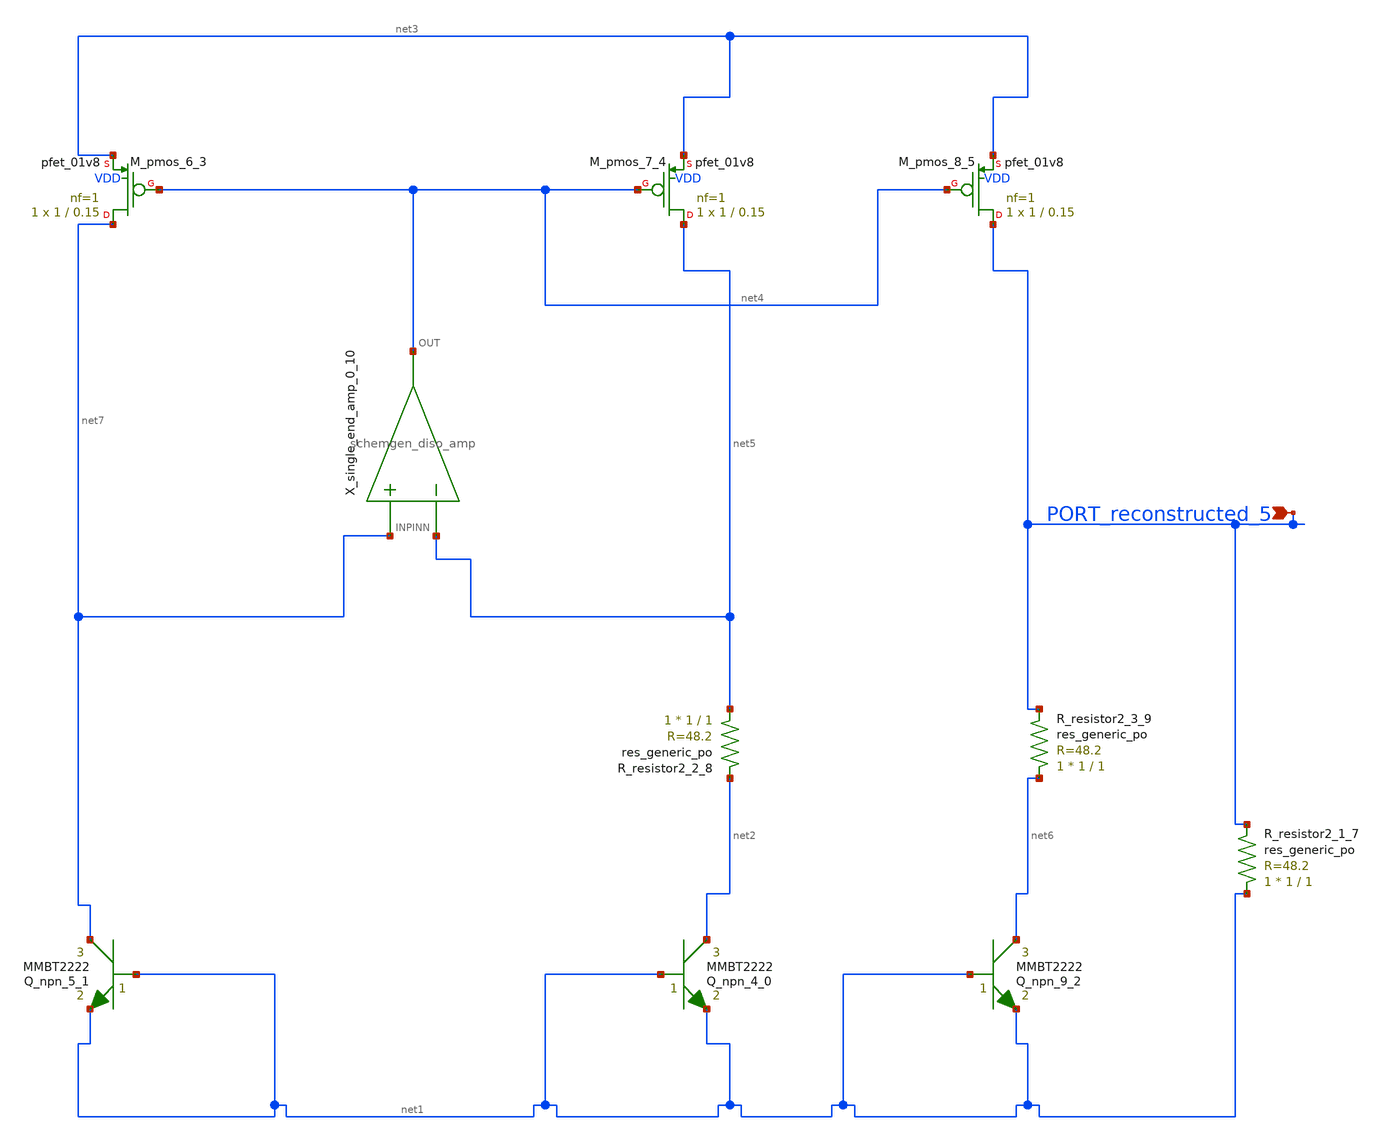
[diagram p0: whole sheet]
** sch_path: schematics/Image2Net/006.sch
**.subckt 006 PORT_reconstructed_5
*.ipin PORT_reconstructed_5
Q_npn_4_0 net2 net1 net1 MMBT2222 area=1 m=1
Q_npn_5_1 net7 net1 net1 MMBT2222 area=1 m=1
Q_npn_9_2 net6 net1 net1 MMBT2222 area=1 m=1
XM_pmos_6_3 net7 net4 net3 VDD sky130_fd_pr__pfet_01v8 L=0.15 W=1 nf=1 ad='int((1 + 1)/2) * 1 / 1 * 0.29'
+ as='int((1 + 2)/2) * 1 / 1 * 0.29' pd='2*int((1 + 1)/2) * (1 / 1 + 0.29)' ps='2*int((1 + 2)/2) * (1 / 1 + 0.29)'
+ nrd='0.29 / 1 ' nrs='0.29 / 1 ' sa=0 sb=0 sd=0 mult=1 m=1
XM_pmos_7_4 net5 net4 net3 VDD sky130_fd_pr__pfet_01v8 L=0.15 W=1 nf=1 ad='int((1 + 1)/2) * 1 / 1 * 0.29'
+ as='int((1 + 2)/2) * 1 / 1 * 0.29' pd='2*int((1 + 1)/2) * (1 / 1 + 0.29)' ps='2*int((1 + 2)/2) * (1 / 1 + 0.29)'
+ nrd='0.29 / 1 ' nrs='0.29 / 1 ' sa=0 sb=0 sd=0 mult=1 m=1
XM_pmos_8_5 PORT_reconstructed_5 net4 net3 VDD sky130_fd_pr__pfet_01v8 L=0.15 W=1 nf=1 ad='int((1 + 1)/2) * 1 / 1 * 0.29'
+ as='int((1 + 2)/2) * 1 / 1 * 0.29' pd='2*int((1 + 1)/2) * (1 / 1 + 0.29)' ps='2*int((1 + 2)/2) * (1 / 1 + 0.29)'
+ nrd='0.29 / 1 ' nrs='0.29 / 1 ' sa=0 sb=0 sd=0 mult=1 m=1
XR_resistor2_1_7 net1 PORT_reconstructed_5 sky130_fd_pr__res_generic_po W=1 L=1 m=1
XR_resistor2_2_8 net5 net2 sky130_fd_pr__res_generic_po W=1 L=1 m=1
XR_resistor2_3_9 net6 PORT_reconstructed_5 sky130_fd_pr__res_generic_po W=1 L=1 m=1
X_single_end_amp_0_10 net7 net5 net4 schemgen_diso_amp
**.ends

* expanding   symbol:  schemgen_diso_amp.sym # of pins=3
** sym_path: symbols/schemgen_diso_amp.sym
.subckt schemgen_diso_amp INP INN OUT
* SchemGen ideal op-amp: Vout = 1e5 * (V(INP) - V(INN))
E1 OUT 0 INP INN 1e5
.ends schemgen_diso_amp
.end
